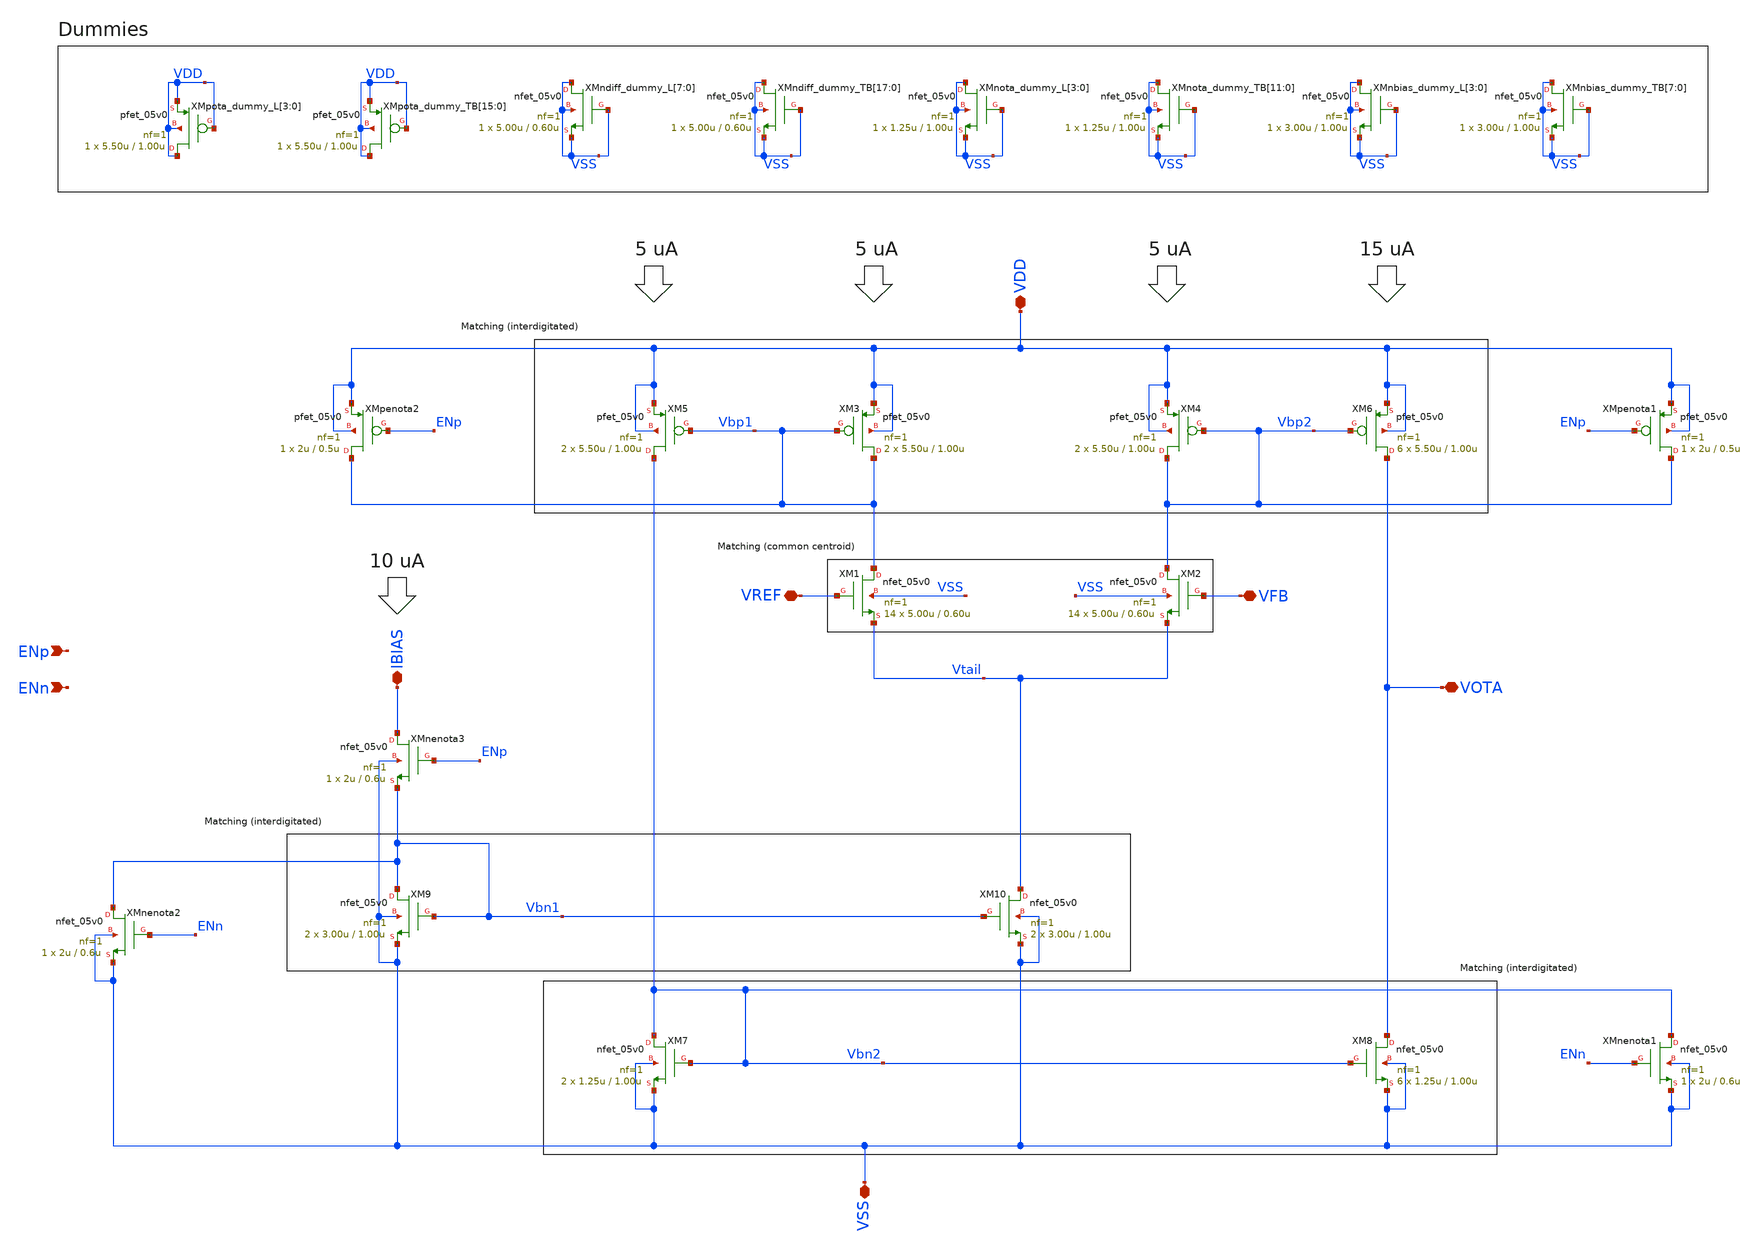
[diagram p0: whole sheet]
** sch_path: designs/libs/core_ldo/ldo_OTA/ldo_OTA.sch
**.subckt ldo_OTA VDD VSS VOTA VREF IBIAS VFB ENp ENn
*.iopin VDD
*.iopin VSS
*.iopin VOTA
*.iopin VREF
*.iopin IBIAS
*.iopin VFB
*.ipin ENp
*.ipin ENn
XM3 Vbp1 Vbp1 VDD VDD pfet_05v0 L=1.00u W=5.50u nf=1 ad='int((nf+1)/2) * W/nf * 0.18u' as='int((nf+2)/2) * W/nf * 0.18u'
+ pd='2*int((nf+1)/2) * (W/nf + 0.18u)' ps='2*int((nf+2)/2) * (W/nf + 0.18u)' nrd='0.18u / W' nrs='0.18u / W'
+ sa=0 sb=0 sd=0 m=2
XM4 Vbp2 Vbp2 VDD VDD pfet_05v0 L=1.00u W=5.50u nf=1 ad='int((nf+1)/2) * W/nf * 0.18u' as='int((nf+2)/2) * W/nf * 0.18u'
+ pd='2*int((nf+1)/2) * (W/nf + 0.18u)' ps='2*int((nf+2)/2) * (W/nf + 0.18u)' nrd='0.18u / W' nrs='0.18u / W'
+ sa=0 sb=0 sd=0 m=2
XM5 Vbn2 Vbp1 VDD VDD pfet_05v0 L=1.00u W=5.50u nf=1 ad='int((nf+1)/2) * W/nf * 0.18u' as='int((nf+2)/2) * W/nf * 0.18u'
+ pd='2*int((nf+1)/2) * (W/nf + 0.18u)' ps='2*int((nf+2)/2) * (W/nf + 0.18u)' nrd='0.18u / W' nrs='0.18u / W'
+ sa=0 sb=0 sd=0 m=2
XM6 VOTA Vbp2 VDD VDD pfet_05v0 L=1.00u W=5.50u nf=1 ad='int((nf+1)/2) * W/nf * 0.18u' as='int((nf+2)/2) * W/nf * 0.18u'
+ pd='2*int((nf+1)/2) * (W/nf + 0.18u)' ps='2*int((nf+2)/2) * (W/nf + 0.18u)' nrd='0.18u / W' nrs='0.18u / W'
+ sa=0 sb=0 sd=0 m=6
XM9 Vbn1 Vbn1 VSS VSS nfet_05v0 L=1.00u W=3.00u nf=1 ad='int((nf+1)/2) * W/nf * 0.18u' as='int((nf+2)/2) * W/nf * 0.18u'
+ pd='2*int((nf+1)/2) * (W/nf + 0.18u)' ps='2*int((nf+2)/2) * (W/nf + 0.18u)' nrd='0.18u / W' nrs='0.18u / W'
+ sa=0 sb=0 sd=0 m=2
XM10 Vtail Vbn1 VSS VSS nfet_05v0 L=1.00u W=3.00u nf=1 ad='int((nf+1)/2) * W/nf * 0.18u' as='int((nf+2)/2) * W/nf * 0.18u'
+ pd='2*int((nf+1)/2) * (W/nf + 0.18u)' ps='2*int((nf+2)/2) * (W/nf + 0.18u)' nrd='0.18u / W' nrs='0.18u / W'
+ sa=0 sb=0 sd=0 m=2
XM7 Vbn2 Vbn2 VSS VSS nfet_05v0 L=1.00u W=1.25u nf=1 ad='int((nf+1)/2) * W/nf * 0.18u' as='int((nf+2)/2) * W/nf * 0.18u'
+ pd='2*int((nf+1)/2) * (W/nf + 0.18u)' ps='2*int((nf+2)/2) * (W/nf + 0.18u)' nrd='0.18u / W' nrs='0.18u / W'
+ sa=0 sb=0 sd=0 m=2
XM8 VOTA Vbn2 VSS VSS nfet_05v0 L=1.00u W=1.25u nf=1 ad='int((nf+1)/2) * W/nf * 0.18u' as='int((nf+2)/2) * W/nf * 0.18u'
+ pd='2*int((nf+1)/2) * (W/nf + 0.18u)' ps='2*int((nf+2)/2) * (W/nf + 0.18u)' nrd='0.18u / W' nrs='0.18u / W'
+ sa=0 sb=0 sd=0 m=6
XM1 Vbp1 VREF Vtail VSS nfet_05v0 L=0.60u W=5.00u nf=1 ad='int((nf+1)/2) * W/nf * 0.18u' as='int((nf+2)/2) * W/nf * 0.18u'
+ pd='2*int((nf+1)/2) * (W/nf + 0.18u)' ps='2*int((nf+2)/2) * (W/nf + 0.18u)' nrd='0.18u / W' nrs='0.18u / W'
+ sa=0 sb=0 sd=0 m=14
XM2 Vbp2 VFB Vtail VSS nfet_05v0 L=0.60u W=5.00u nf=1 ad='int((nf+1)/2) * W/nf * 0.18u' as='int((nf+2)/2) * W/nf * 0.18u'
+ pd='2*int((nf+1)/2) * (W/nf + 0.18u)' ps='2*int((nf+2)/2) * (W/nf + 0.18u)' nrd='0.18u / W' nrs='0.18u / W'
+ sa=0 sb=0 sd=0 m=14
XMpota_dummy_L[3] VDD VDD VDD VDD pfet_05v0 L=1.00u W=5.50u nf=1 ad='int((nf+1)/2) * W/nf * 0.18u' as='int((nf+2)/2) * W/nf * 0.18u'
+ pd='2*int((nf+1)/2) * (W/nf + 0.18u)' ps='2*int((nf+2)/2) * (W/nf + 0.18u)' nrd='0.18u / W' nrs='0.18u / W'
+ sa=0 sb=0 sd=0 m=1
XMpota_dummy_L[2] VDD VDD VDD VDD pfet_05v0 L=1.00u W=5.50u nf=1 ad='int((nf+1)/2) * W/nf * 0.18u' as='int((nf+2)/2) * W/nf * 0.18u'
+ pd='2*int((nf+1)/2) * (W/nf + 0.18u)' ps='2*int((nf+2)/2) * (W/nf + 0.18u)' nrd='0.18u / W' nrs='0.18u / W'
+ sa=0 sb=0 sd=0 m=1
XMpota_dummy_L[1] VDD VDD VDD VDD pfet_05v0 L=1.00u W=5.50u nf=1 ad='int((nf+1)/2) * W/nf * 0.18u' as='int((nf+2)/2) * W/nf * 0.18u'
+ pd='2*int((nf+1)/2) * (W/nf + 0.18u)' ps='2*int((nf+2)/2) * (W/nf + 0.18u)' nrd='0.18u / W' nrs='0.18u / W'
+ sa=0 sb=0 sd=0 m=1
XMpota_dummy_L[0] VDD VDD VDD VDD pfet_05v0 L=1.00u W=5.50u nf=1 ad='int((nf+1)/2) * W/nf * 0.18u' as='int((nf+2)/2) * W/nf * 0.18u'
+ pd='2*int((nf+1)/2) * (W/nf + 0.18u)' ps='2*int((nf+2)/2) * (W/nf + 0.18u)' nrd='0.18u / W' nrs='0.18u / W'
+ sa=0 sb=0 sd=0 m=1
XMpota_dummy_TB[15] VDD VDD VDD VDD pfet_05v0 L=1.00u W=5.50u nf=1 ad='int((nf+1)/2) * W/nf * 0.18u'
+ as='int((nf+2)/2) * W/nf * 0.18u' pd='2*int((nf+1)/2) * (W/nf + 0.18u)' ps='2*int((nf+2)/2) * (W/nf + 0.18u)'
+ nrd='0.18u / W' nrs='0.18u / W' sa=0 sb=0 sd=0 m=1
XMpota_dummy_TB[14] VDD VDD VDD VDD pfet_05v0 L=1.00u W=5.50u nf=1 ad='int((nf+1)/2) * W/nf * 0.18u'
+ as='int((nf+2)/2) * W/nf * 0.18u' pd='2*int((nf+1)/2) * (W/nf + 0.18u)' ps='2*int((nf+2)/2) * (W/nf + 0.18u)'
+ nrd='0.18u / W' nrs='0.18u / W' sa=0 sb=0 sd=0 m=1
XMpota_dummy_TB[13] VDD VDD VDD VDD pfet_05v0 L=1.00u W=5.50u nf=1 ad='int((nf+1)/2) * W/nf * 0.18u'
+ as='int((nf+2)/2) * W/nf * 0.18u' pd='2*int((nf+1)/2) * (W/nf + 0.18u)' ps='2*int((nf+2)/2) * (W/nf + 0.18u)'
+ nrd='0.18u / W' nrs='0.18u / W' sa=0 sb=0 sd=0 m=1
XMpota_dummy_TB[12] VDD VDD VDD VDD pfet_05v0 L=1.00u W=5.50u nf=1 ad='int((nf+1)/2) * W/nf * 0.18u'
+ as='int((nf+2)/2) * W/nf * 0.18u' pd='2*int((nf+1)/2) * (W/nf + 0.18u)' ps='2*int((nf+2)/2) * (W/nf + 0.18u)'
+ nrd='0.18u / W' nrs='0.18u / W' sa=0 sb=0 sd=0 m=1
XMpota_dummy_TB[11] VDD VDD VDD VDD pfet_05v0 L=1.00u W=5.50u nf=1 ad='int((nf+1)/2) * W/nf * 0.18u'
+ as='int((nf+2)/2) * W/nf * 0.18u' pd='2*int((nf+1)/2) * (W/nf + 0.18u)' ps='2*int((nf+2)/2) * (W/nf + 0.18u)'
+ nrd='0.18u / W' nrs='0.18u / W' sa=0 sb=0 sd=0 m=1
XMpota_dummy_TB[10] VDD VDD VDD VDD pfet_05v0 L=1.00u W=5.50u nf=1 ad='int((nf+1)/2) * W/nf * 0.18u'
+ as='int((nf+2)/2) * W/nf * 0.18u' pd='2*int((nf+1)/2) * (W/nf + 0.18u)' ps='2*int((nf+2)/2) * (W/nf + 0.18u)'
+ nrd='0.18u / W' nrs='0.18u / W' sa=0 sb=0 sd=0 m=1
XMpota_dummy_TB[9] VDD VDD VDD VDD pfet_05v0 L=1.00u W=5.50u nf=1 ad='int((nf+1)/2) * W/nf * 0.18u' as='int((nf+2)/2) * W/nf * 0.18u'
+ pd='2*int((nf+1)/2) * (W/nf + 0.18u)' ps='2*int((nf+2)/2) * (W/nf + 0.18u)' nrd='0.18u / W' nrs='0.18u / W'
+ sa=0 sb=0 sd=0 m=1
XMpota_dummy_TB[8] VDD VDD VDD VDD pfet_05v0 L=1.00u W=5.50u nf=1 ad='int((nf+1)/2) * W/nf * 0.18u' as='int((nf+2)/2) * W/nf * 0.18u'
+ pd='2*int((nf+1)/2) * (W/nf + 0.18u)' ps='2*int((nf+2)/2) * (W/nf + 0.18u)' nrd='0.18u / W' nrs='0.18u / W'
+ sa=0 sb=0 sd=0 m=1
XMpota_dummy_TB[7] VDD VDD VDD VDD pfet_05v0 L=1.00u W=5.50u nf=1 ad='int((nf+1)/2) * W/nf * 0.18u' as='int((nf+2)/2) * W/nf * 0.18u'
+ pd='2*int((nf+1)/2) * (W/nf + 0.18u)' ps='2*int((nf+2)/2) * (W/nf + 0.18u)' nrd='0.18u / W' nrs='0.18u / W'
+ sa=0 sb=0 sd=0 m=1
XMpota_dummy_TB[6] VDD VDD VDD VDD pfet_05v0 L=1.00u W=5.50u nf=1 ad='int((nf+1)/2) * W/nf * 0.18u' as='int((nf+2)/2) * W/nf * 0.18u'
+ pd='2*int((nf+1)/2) * (W/nf + 0.18u)' ps='2*int((nf+2)/2) * (W/nf + 0.18u)' nrd='0.18u / W' nrs='0.18u / W'
+ sa=0 sb=0 sd=0 m=1
XMpota_dummy_TB[5] VDD VDD VDD VDD pfet_05v0 L=1.00u W=5.50u nf=1 ad='int((nf+1)/2) * W/nf * 0.18u' as='int((nf+2)/2) * W/nf * 0.18u'
+ pd='2*int((nf+1)/2) * (W/nf + 0.18u)' ps='2*int((nf+2)/2) * (W/nf + 0.18u)' nrd='0.18u / W' nrs='0.18u / W'
+ sa=0 sb=0 sd=0 m=1
XMpota_dummy_TB[4] VDD VDD VDD VDD pfet_05v0 L=1.00u W=5.50u nf=1 ad='int((nf+1)/2) * W/nf * 0.18u' as='int((nf+2)/2) * W/nf * 0.18u'
+ pd='2*int((nf+1)/2) * (W/nf + 0.18u)' ps='2*int((nf+2)/2) * (W/nf + 0.18u)' nrd='0.18u / W' nrs='0.18u / W'
+ sa=0 sb=0 sd=0 m=1
XMpota_dummy_TB[3] VDD VDD VDD VDD pfet_05v0 L=1.00u W=5.50u nf=1 ad='int((nf+1)/2) * W/nf * 0.18u' as='int((nf+2)/2) * W/nf * 0.18u'
+ pd='2*int((nf+1)/2) * (W/nf + 0.18u)' ps='2*int((nf+2)/2) * (W/nf + 0.18u)' nrd='0.18u / W' nrs='0.18u / W'
+ sa=0 sb=0 sd=0 m=1
XMpota_dummy_TB[2] VDD VDD VDD VDD pfet_05v0 L=1.00u W=5.50u nf=1 ad='int((nf+1)/2) * W/nf * 0.18u' as='int((nf+2)/2) * W/nf * 0.18u'
+ pd='2*int((nf+1)/2) * (W/nf + 0.18u)' ps='2*int((nf+2)/2) * (W/nf + 0.18u)' nrd='0.18u / W' nrs='0.18u / W'
+ sa=0 sb=0 sd=0 m=1
XMpota_dummy_TB[1] VDD VDD VDD VDD pfet_05v0 L=1.00u W=5.50u nf=1 ad='int((nf+1)/2) * W/nf * 0.18u' as='int((nf+2)/2) * W/nf * 0.18u'
+ pd='2*int((nf+1)/2) * (W/nf + 0.18u)' ps='2*int((nf+2)/2) * (W/nf + 0.18u)' nrd='0.18u / W' nrs='0.18u / W'
+ sa=0 sb=0 sd=0 m=1
XMpota_dummy_TB[0] VDD VDD VDD VDD pfet_05v0 L=1.00u W=5.50u nf=1 ad='int((nf+1)/2) * W/nf * 0.18u' as='int((nf+2)/2) * W/nf * 0.18u'
+ pd='2*int((nf+1)/2) * (W/nf + 0.18u)' ps='2*int((nf+2)/2) * (W/nf + 0.18u)' nrd='0.18u / W' nrs='0.18u / W'
+ sa=0 sb=0 sd=0 m=1
XMndiff_dummy_L[7] VSS VSS VSS VSS nfet_05v0 L=0.60u W=5.00u nf=1 ad='int((nf+1)/2) * W/nf * 0.18u' as='int((nf+2)/2) * W/nf * 0.18u'
+ pd='2*int((nf+1)/2) * (W/nf + 0.18u)' ps='2*int((nf+2)/2) * (W/nf + 0.18u)' nrd='0.18u / W' nrs='0.18u / W'
+ sa=0 sb=0 sd=0 m=1
XMndiff_dummy_L[6] VSS VSS VSS VSS nfet_05v0 L=0.60u W=5.00u nf=1 ad='int((nf+1)/2) * W/nf * 0.18u' as='int((nf+2)/2) * W/nf * 0.18u'
+ pd='2*int((nf+1)/2) * (W/nf + 0.18u)' ps='2*int((nf+2)/2) * (W/nf + 0.18u)' nrd='0.18u / W' nrs='0.18u / W'
+ sa=0 sb=0 sd=0 m=1
XMndiff_dummy_L[5] VSS VSS VSS VSS nfet_05v0 L=0.60u W=5.00u nf=1 ad='int((nf+1)/2) * W/nf * 0.18u' as='int((nf+2)/2) * W/nf * 0.18u'
+ pd='2*int((nf+1)/2) * (W/nf + 0.18u)' ps='2*int((nf+2)/2) * (W/nf + 0.18u)' nrd='0.18u / W' nrs='0.18u / W'
+ sa=0 sb=0 sd=0 m=1
XMndiff_dummy_L[4] VSS VSS VSS VSS nfet_05v0 L=0.60u W=5.00u nf=1 ad='int((nf+1)/2) * W/nf * 0.18u' as='int((nf+2)/2) * W/nf * 0.18u'
+ pd='2*int((nf+1)/2) * (W/nf + 0.18u)' ps='2*int((nf+2)/2) * (W/nf + 0.18u)' nrd='0.18u / W' nrs='0.18u / W'
+ sa=0 sb=0 sd=0 m=1
XMndiff_dummy_L[3] VSS VSS VSS VSS nfet_05v0 L=0.60u W=5.00u nf=1 ad='int((nf+1)/2) * W/nf * 0.18u' as='int((nf+2)/2) * W/nf * 0.18u'
+ pd='2*int((nf+1)/2) * (W/nf + 0.18u)' ps='2*int((nf+2)/2) * (W/nf + 0.18u)' nrd='0.18u / W' nrs='0.18u / W'
+ sa=0 sb=0 sd=0 m=1
XMndiff_dummy_L[2] VSS VSS VSS VSS nfet_05v0 L=0.60u W=5.00u nf=1 ad='int((nf+1)/2) * W/nf * 0.18u' as='int((nf+2)/2) * W/nf * 0.18u'
+ pd='2*int((nf+1)/2) * (W/nf + 0.18u)' ps='2*int((nf+2)/2) * (W/nf + 0.18u)' nrd='0.18u / W' nrs='0.18u / W'
+ sa=0 sb=0 sd=0 m=1
XMndiff_dummy_L[1] VSS VSS VSS VSS nfet_05v0 L=0.60u W=5.00u nf=1 ad='int((nf+1)/2) * W/nf * 0.18u' as='int((nf+2)/2) * W/nf * 0.18u'
+ pd='2*int((nf+1)/2) * (W/nf + 0.18u)' ps='2*int((nf+2)/2) * (W/nf + 0.18u)' nrd='0.18u / W' nrs='0.18u / W'
+ sa=0 sb=0 sd=0 m=1
XMndiff_dummy_L[0] VSS VSS VSS VSS nfet_05v0 L=0.60u W=5.00u nf=1 ad='int((nf+1)/2) * W/nf * 0.18u' as='int((nf+2)/2) * W/nf * 0.18u'
+ pd='2*int((nf+1)/2) * (W/nf + 0.18u)' ps='2*int((nf+2)/2) * (W/nf + 0.18u)' nrd='0.18u / W' nrs='0.18u / W'
+ sa=0 sb=0 sd=0 m=1
XMndiff_dummy_TB[17] VSS VSS VSS VSS nfet_05v0 L=0.60u W=5.00u nf=1 ad='int((nf+1)/2) * W/nf * 0.18u'
+ as='int((nf+2)/2) * W/nf * 0.18u' pd='2*int((nf+1)/2) * (W/nf + 0.18u)' ps='2*int((nf+2)/2) * (W/nf + 0.18u)'
+ nrd='0.18u / W' nrs='0.18u / W' sa=0 sb=0 sd=0 m=1
XMndiff_dummy_TB[16] VSS VSS VSS VSS nfet_05v0 L=0.60u W=5.00u nf=1 ad='int((nf+1)/2) * W/nf * 0.18u'
+ as='int((nf+2)/2) * W/nf * 0.18u' pd='2*int((nf+1)/2) * (W/nf + 0.18u)' ps='2*int((nf+2)/2) * (W/nf + 0.18u)'
+ nrd='0.18u / W' nrs='0.18u / W' sa=0 sb=0 sd=0 m=1
XMndiff_dummy_TB[15] VSS VSS VSS VSS nfet_05v0 L=0.60u W=5.00u nf=1 ad='int((nf+1)/2) * W/nf * 0.18u'
+ as='int((nf+2)/2) * W/nf * 0.18u' pd='2*int((nf+1)/2) * (W/nf + 0.18u)' ps='2*int((nf+2)/2) * (W/nf + 0.18u)'
+ nrd='0.18u / W' nrs='0.18u / W' sa=0 sb=0 sd=0 m=1
XMndiff_dummy_TB[14] VSS VSS VSS VSS nfet_05v0 L=0.60u W=5.00u nf=1 ad='int((nf+1)/2) * W/nf * 0.18u'
+ as='int((nf+2)/2) * W/nf * 0.18u' pd='2*int((nf+1)/2) * (W/nf + 0.18u)' ps='2*int((nf+2)/2) * (W/nf + 0.18u)'
+ nrd='0.18u / W' nrs='0.18u / W' sa=0 sb=0 sd=0 m=1
XMndiff_dummy_TB[13] VSS VSS VSS VSS nfet_05v0 L=0.60u W=5.00u nf=1 ad='int((nf+1)/2) * W/nf * 0.18u'
+ as='int((nf+2)/2) * W/nf * 0.18u' pd='2*int((nf+1)/2) * (W/nf + 0.18u)' ps='2*int((nf+2)/2) * (W/nf + 0.18u)'
+ nrd='0.18u / W' nrs='0.18u / W' sa=0 sb=0 sd=0 m=1
XMndiff_dummy_TB[12] VSS VSS VSS VSS nfet_05v0 L=0.60u W=5.00u nf=1 ad='int((nf+1)/2) * W/nf * 0.18u'
+ as='int((nf+2)/2) * W/nf * 0.18u' pd='2*int((nf+1)/2) * (W/nf + 0.18u)' ps='2*int((nf+2)/2) * (W/nf + 0.18u)'
+ nrd='0.18u / W' nrs='0.18u / W' sa=0 sb=0 sd=0 m=1
XMndiff_dummy_TB[11] VSS VSS VSS VSS nfet_05v0 L=0.60u W=5.00u nf=1 ad='int((nf+1)/2) * W/nf * 0.18u'
+ as='int((nf+2)/2) * W/nf * 0.18u' pd='2*int((nf+1)/2) * (W/nf + 0.18u)' ps='2*int((nf+2)/2) * (W/nf + 0.18u)'
+ nrd='0.18u / W' nrs='0.18u / W' sa=0 sb=0 sd=0 m=1
XMndiff_dummy_TB[10] VSS VSS VSS VSS nfet_05v0 L=0.60u W=5.00u nf=1 ad='int((nf+1)/2) * W/nf * 0.18u'
+ as='int((nf+2)/2) * W/nf * 0.18u' pd='2*int((nf+1)/2) * (W/nf + 0.18u)' ps='2*int((nf+2)/2) * (W/nf + 0.18u)'
+ nrd='0.18u / W' nrs='0.18u / W' sa=0 sb=0 sd=0 m=1
XMndiff_dummy_TB[9] VSS VSS VSS VSS nfet_05v0 L=0.60u W=5.00u nf=1 ad='int((nf+1)/2) * W/nf * 0.18u'
+ as='int((nf+2)/2) * W/nf * 0.18u' pd='2*int((nf+1)/2) * (W/nf + 0.18u)' ps='2*int((nf+2)/2) * (W/nf + 0.18u)'
+ nrd='0.18u / W' nrs='0.18u / W' sa=0 sb=0 sd=0 m=1
XMndiff_dummy_TB[8] VSS VSS VSS VSS nfet_05v0 L=0.60u W=5.00u nf=1 ad='int((nf+1)/2) * W/nf * 0.18u'
+ as='int((nf+2)/2) * W/nf * 0.18u' pd='2*int((nf+1)/2) * (W/nf + 0.18u)' ps='2*int((nf+2)/2) * (W/nf + 0.18u)'
+ nrd='0.18u / W' nrs='0.18u / W' sa=0 sb=0 sd=0 m=1
XMndiff_dummy_TB[7] VSS VSS VSS VSS nfet_05v0 L=0.60u W=5.00u nf=1 ad='int((nf+1)/2) * W/nf * 0.18u'
+ as='int((nf+2)/2) * W/nf * 0.18u' pd='2*int((nf+1)/2) * (W/nf + 0.18u)' ps='2*int((nf+2)/2) * (W/nf + 0.18u)'
+ nrd='0.18u / W' nrs='0.18u / W' sa=0 sb=0 sd=0 m=1
XMndiff_dummy_TB[6] VSS VSS VSS VSS nfet_05v0 L=0.60u W=5.00u nf=1 ad='int((nf+1)/2) * W/nf * 0.18u'
+ as='int((nf+2)/2) * W/nf * 0.18u' pd='2*int((nf+1)/2) * (W/nf + 0.18u)' ps='2*int((nf+2)/2) * (W/nf + 0.18u)'
+ nrd='0.18u / W' nrs='0.18u / W' sa=0 sb=0 sd=0 m=1
XMndiff_dummy_TB[5] VSS VSS VSS VSS nfet_05v0 L=0.60u W=5.00u nf=1 ad='int((nf+1)/2) * W/nf * 0.18u'
+ as='int((nf+2)/2) * W/nf * 0.18u' pd='2*int((nf+1)/2) * (W/nf + 0.18u)' ps='2*int((nf+2)/2) * (W/nf + 0.18u)'
+ nrd='0.18u / W' nrs='0.18u / W' sa=0 sb=0 sd=0 m=1
XMndiff_dummy_TB[4] VSS VSS VSS VSS nfet_05v0 L=0.60u W=5.00u nf=1 ad='int((nf+1)/2) * W/nf * 0.18u'
+ as='int((nf+2)/2) * W/nf * 0.18u' pd='2*int((nf+1)/2) * (W/nf + 0.18u)' ps='2*int((nf+2)/2) * (W/nf + 0.18u)'
+ nrd='0.18u / W' nrs='0.18u / W' sa=0 sb=0 sd=0 m=1
XMndiff_dummy_TB[3] VSS VSS VSS VSS nfet_05v0 L=0.60u W=5.00u nf=1 ad='int((nf+1)/2) * W/nf * 0.18u'
+ as='int((nf+2)/2) * W/nf * 0.18u' pd='2*int((nf+1)/2) * (W/nf + 0.18u)' ps='2*int((nf+2)/2) * (W/nf + 0.18u)'
+ nrd='0.18u / W' nrs='0.18u / W' sa=0 sb=0 sd=0 m=1
XMndiff_dummy_TB[2] VSS VSS VSS VSS nfet_05v0 L=0.60u W=5.00u nf=1 ad='int((nf+1)/2) * W/nf * 0.18u'
+ as='int((nf+2)/2) * W/nf * 0.18u' pd='2*int((nf+1)/2) * (W/nf + 0.18u)' ps='2*int((nf+2)/2) * (W/nf + 0.18u)'
+ nrd='0.18u / W' nrs='0.18u / W' sa=0 sb=0 sd=0 m=1
XMndiff_dummy_TB[1] VSS VSS VSS VSS nfet_05v0 L=0.60u W=5.00u nf=1 ad='int((nf+1)/2) * W/nf * 0.18u'
+ as='int((nf+2)/2) * W/nf * 0.18u' pd='2*int((nf+1)/2) * (W/nf + 0.18u)' ps='2*int((nf+2)/2) * (W/nf + 0.18u)'
+ nrd='0.18u / W' nrs='0.18u / W' sa=0 sb=0 sd=0 m=1
XMndiff_dummy_TB[0] VSS VSS VSS VSS nfet_05v0 L=0.60u W=5.00u nf=1 ad='int((nf+1)/2) * W/nf * 0.18u'
+ as='int((nf+2)/2) * W/nf * 0.18u' pd='2*int((nf+1)/2) * (W/nf + 0.18u)' ps='2*int((nf+2)/2) * (W/nf + 0.18u)'
+ nrd='0.18u / W' nrs='0.18u / W' sa=0 sb=0 sd=0 m=1
XMnota_dummy_L[3] VSS VSS VSS VSS nfet_05v0 L=1.00u W=1.25u nf=1 ad='int((nf+1)/2) * W/nf * 0.18u' as='int((nf+2)/2) * W/nf * 0.18u'
+ pd='2*int((nf+1)/2) * (W/nf + 0.18u)' ps='2*int((nf+2)/2) * (W/nf + 0.18u)' nrd='0.18u / W' nrs='0.18u / W'
+ sa=0 sb=0 sd=0 m=1
XMnota_dummy_L[2] VSS VSS VSS VSS nfet_05v0 L=1.00u W=1.25u nf=1 ad='int((nf+1)/2) * W/nf * 0.18u' as='int((nf+2)/2) * W/nf * 0.18u'
+ pd='2*int((nf+1)/2) * (W/nf + 0.18u)' ps='2*int((nf+2)/2) * (W/nf + 0.18u)' nrd='0.18u / W' nrs='0.18u / W'
+ sa=0 sb=0 sd=0 m=1
XMnota_dummy_L[1] VSS VSS VSS VSS nfet_05v0 L=1.00u W=1.25u nf=1 ad='int((nf+1)/2) * W/nf * 0.18u' as='int((nf+2)/2) * W/nf * 0.18u'
+ pd='2*int((nf+1)/2) * (W/nf + 0.18u)' ps='2*int((nf+2)/2) * (W/nf + 0.18u)' nrd='0.18u / W' nrs='0.18u / W'
+ sa=0 sb=0 sd=0 m=1
XMnota_dummy_L[0] VSS VSS VSS VSS nfet_05v0 L=1.00u W=1.25u nf=1 ad='int((nf+1)/2) * W/nf * 0.18u' as='int((nf+2)/2) * W/nf * 0.18u'
+ pd='2*int((nf+1)/2) * (W/nf + 0.18u)' ps='2*int((nf+2)/2) * (W/nf + 0.18u)' nrd='0.18u / W' nrs='0.18u / W'
+ sa=0 sb=0 sd=0 m=1
XMnota_dummy_TB[11] VSS VSS VSS VSS nfet_05v0 L=1.00u W=1.25u nf=1 ad='int((nf+1)/2) * W/nf * 0.18u'
+ as='int((nf+2)/2) * W/nf * 0.18u' pd='2*int((nf+1)/2) * (W/nf + 0.18u)' ps='2*int((nf+2)/2) * (W/nf + 0.18u)'
+ nrd='0.18u / W' nrs='0.18u / W' sa=0 sb=0 sd=0 m=1
XMnota_dummy_TB[10] VSS VSS VSS VSS nfet_05v0 L=1.00u W=1.25u nf=1 ad='int((nf+1)/2) * W/nf * 0.18u'
+ as='int((nf+2)/2) * W/nf * 0.18u' pd='2*int((nf+1)/2) * (W/nf + 0.18u)' ps='2*int((nf+2)/2) * (W/nf + 0.18u)'
+ nrd='0.18u / W' nrs='0.18u / W' sa=0 sb=0 sd=0 m=1
XMnota_dummy_TB[9] VSS VSS VSS VSS nfet_05v0 L=1.00u W=1.25u nf=1 ad='int((nf+1)/2) * W/nf * 0.18u' as='int((nf+2)/2) * W/nf * 0.18u'
+ pd='2*int((nf+1)/2) * (W/nf + 0.18u)' ps='2*int((nf+2)/2) * (W/nf + 0.18u)' nrd='0.18u / W' nrs='0.18u / W'
+ sa=0 sb=0 sd=0 m=1
XMnota_dummy_TB[8] VSS VSS VSS VSS nfet_05v0 L=1.00u W=1.25u nf=1 ad='int((nf+1)/2) * W/nf * 0.18u' as='int((nf+2)/2) * W/nf * 0.18u'
+ pd='2*int((nf+1)/2) * (W/nf + 0.18u)' ps='2*int((nf+2)/2) * (W/nf + 0.18u)' nrd='0.18u / W' nrs='0.18u / W'
+ sa=0 sb=0 sd=0 m=1
XMnota_dummy_TB[7] VSS VSS VSS VSS nfet_05v0 L=1.00u W=1.25u nf=1 ad='int((nf+1)/2) * W/nf * 0.18u' as='int((nf+2)/2) * W/nf * 0.18u'
+ pd='2*int((nf+1)/2) * (W/nf + 0.18u)' ps='2*int((nf+2)/2) * (W/nf + 0.18u)' nrd='0.18u / W' nrs='0.18u / W'
+ sa=0 sb=0 sd=0 m=1
XMnota_dummy_TB[6] VSS VSS VSS VSS nfet_05v0 L=1.00u W=1.25u nf=1 ad='int((nf+1)/2) * W/nf * 0.18u' as='int((nf+2)/2) * W/nf * 0.18u'
+ pd='2*int((nf+1)/2) * (W/nf + 0.18u)' ps='2*int((nf+2)/2) * (W/nf + 0.18u)' nrd='0.18u / W' nrs='0.18u / W'
+ sa=0 sb=0 sd=0 m=1
XMnota_dummy_TB[5] VSS VSS VSS VSS nfet_05v0 L=1.00u W=1.25u nf=1 ad='int((nf+1)/2) * W/nf * 0.18u' as='int((nf+2)/2) * W/nf * 0.18u'
+ pd='2*int((nf+1)/2) * (W/nf + 0.18u)' ps='2*int((nf+2)/2) * (W/nf + 0.18u)' nrd='0.18u / W' nrs='0.18u / W'
+ sa=0 sb=0 sd=0 m=1
XMnota_dummy_TB[4] VSS VSS VSS VSS nfet_05v0 L=1.00u W=1.25u nf=1 ad='int((nf+1)/2) * W/nf * 0.18u' as='int((nf+2)/2) * W/nf * 0.18u'
+ pd='2*int((nf+1)/2) * (W/nf + 0.18u)' ps='2*int((nf+2)/2) * (W/nf + 0.18u)' nrd='0.18u / W' nrs='0.18u / W'
+ sa=0 sb=0 sd=0 m=1
XMnota_dummy_TB[3] VSS VSS VSS VSS nfet_05v0 L=1.00u W=1.25u nf=1 ad='int((nf+1)/2) * W/nf * 0.18u' as='int((nf+2)/2) * W/nf * 0.18u'
+ pd='2*int((nf+1)/2) * (W/nf + 0.18u)' ps='2*int((nf+2)/2) * (W/nf + 0.18u)' nrd='0.18u / W' nrs='0.18u / W'
+ sa=0 sb=0 sd=0 m=1
XMnota_dummy_TB[2] VSS VSS VSS VSS nfet_05v0 L=1.00u W=1.25u nf=1 ad='int((nf+1)/2) * W/nf * 0.18u' as='int((nf+2)/2) * W/nf * 0.18u'
+ pd='2*int((nf+1)/2) * (W/nf + 0.18u)' ps='2*int((nf+2)/2) * (W/nf + 0.18u)' nrd='0.18u / W' nrs='0.18u / W'
+ sa=0 sb=0 sd=0 m=1
XMnota_dummy_TB[1] VSS VSS VSS VSS nfet_05v0 L=1.00u W=1.25u nf=1 ad='int((nf+1)/2) * W/nf * 0.18u' as='int((nf+2)/2) * W/nf * 0.18u'
+ pd='2*int((nf+1)/2) * (W/nf + 0.18u)' ps='2*int((nf+2)/2) * (W/nf + 0.18u)' nrd='0.18u / W' nrs='0.18u / W'
+ sa=0 sb=0 sd=0 m=1
XMnota_dummy_TB[0] VSS VSS VSS VSS nfet_05v0 L=1.00u W=1.25u nf=1 ad='int((nf+1)/2) * W/nf * 0.18u' as='int((nf+2)/2) * W/nf * 0.18u'
+ pd='2*int((nf+1)/2) * (W/nf + 0.18u)' ps='2*int((nf+2)/2) * (W/nf + 0.18u)' nrd='0.18u / W' nrs='0.18u / W'
+ sa=0 sb=0 sd=0 m=1
XMnbias_dummy_L[3] VSS VSS VSS VSS nfet_05v0 L=1.00u W=3.00u nf=1 ad='int((nf+1)/2) * W/nf * 0.18u' as='int((nf+2)/2) * W/nf * 0.18u'
+ pd='2*int((nf+1)/2) * (W/nf + 0.18u)' ps='2*int((nf+2)/2) * (W/nf + 0.18u)' nrd='0.18u / W' nrs='0.18u / W'
+ sa=0 sb=0 sd=0 m=1
XMnbias_dummy_L[2] VSS VSS VSS VSS nfet_05v0 L=1.00u W=3.00u nf=1 ad='int((nf+1)/2) * W/nf * 0.18u' as='int((nf+2)/2) * W/nf * 0.18u'
+ pd='2*int((nf+1)/2) * (W/nf + 0.18u)' ps='2*int((nf+2)/2) * (W/nf + 0.18u)' nrd='0.18u / W' nrs='0.18u / W'
+ sa=0 sb=0 sd=0 m=1
XMnbias_dummy_L[1] VSS VSS VSS VSS nfet_05v0 L=1.00u W=3.00u nf=1 ad='int((nf+1)/2) * W/nf * 0.18u' as='int((nf+2)/2) * W/nf * 0.18u'
+ pd='2*int((nf+1)/2) * (W/nf + 0.18u)' ps='2*int((nf+2)/2) * (W/nf + 0.18u)' nrd='0.18u / W' nrs='0.18u / W'
+ sa=0 sb=0 sd=0 m=1
XMnbias_dummy_L[0] VSS VSS VSS VSS nfet_05v0 L=1.00u W=3.00u nf=1 ad='int((nf+1)/2) * W/nf * 0.18u' as='int((nf+2)/2) * W/nf * 0.18u'
+ pd='2*int((nf+1)/2) * (W/nf + 0.18u)' ps='2*int((nf+2)/2) * (W/nf + 0.18u)' nrd='0.18u / W' nrs='0.18u / W'
+ sa=0 sb=0 sd=0 m=1
XMnbias_dummy_TB[7] VSS VSS VSS VSS nfet_05v0 L=1.00u W=3.00u nf=1 ad='int((nf+1)/2) * W/nf * 0.18u'
+ as='int((nf+2)/2) * W/nf * 0.18u' pd='2*int((nf+1)/2) * (W/nf + 0.18u)' ps='2*int((nf+2)/2) * (W/nf + 0.18u)'
+ nrd='0.18u / W' nrs='0.18u / W' sa=0 sb=0 sd=0 m=1
XMnbias_dummy_TB[6] VSS VSS VSS VSS nfet_05v0 L=1.00u W=3.00u nf=1 ad='int((nf+1)/2) * W/nf * 0.18u'
+ as='int((nf+2)/2) * W/nf * 0.18u' pd='2*int((nf+1)/2) * (W/nf + 0.18u)' ps='2*int((nf+2)/2) * (W/nf + 0.18u)'
+ nrd='0.18u / W' nrs='0.18u / W' sa=0 sb=0 sd=0 m=1
XMnbias_dummy_TB[5] VSS VSS VSS VSS nfet_05v0 L=1.00u W=3.00u nf=1 ad='int((nf+1)/2) * W/nf * 0.18u'
+ as='int((nf+2)/2) * W/nf * 0.18u' pd='2*int((nf+1)/2) * (W/nf + 0.18u)' ps='2*int((nf+2)/2) * (W/nf + 0.18u)'
+ nrd='0.18u / W' nrs='0.18u / W' sa=0 sb=0 sd=0 m=1
XMnbias_dummy_TB[4] VSS VSS VSS VSS nfet_05v0 L=1.00u W=3.00u nf=1 ad='int((nf+1)/2) * W/nf * 0.18u'
+ as='int((nf+2)/2) * W/nf * 0.18u' pd='2*int((nf+1)/2) * (W/nf + 0.18u)' ps='2*int((nf+2)/2) * (W/nf + 0.18u)'
+ nrd='0.18u / W' nrs='0.18u / W' sa=0 sb=0 sd=0 m=1
XMnbias_dummy_TB[3] VSS VSS VSS VSS nfet_05v0 L=1.00u W=3.00u nf=1 ad='int((nf+1)/2) * W/nf * 0.18u'
+ as='int((nf+2)/2) * W/nf * 0.18u' pd='2*int((nf+1)/2) * (W/nf + 0.18u)' ps='2*int((nf+2)/2) * (W/nf + 0.18u)'
+ nrd='0.18u / W' nrs='0.18u / W' sa=0 sb=0 sd=0 m=1
XMnbias_dummy_TB[2] VSS VSS VSS VSS nfet_05v0 L=1.00u W=3.00u nf=1 ad='int((nf+1)/2) * W/nf * 0.18u'
+ as='int((nf+2)/2) * W/nf * 0.18u' pd='2*int((nf+1)/2) * (W/nf + 0.18u)' ps='2*int((nf+2)/2) * (W/nf + 0.18u)'
+ nrd='0.18u / W' nrs='0.18u / W' sa=0 sb=0 sd=0 m=1
XMnbias_dummy_TB[1] VSS VSS VSS VSS nfet_05v0 L=1.00u W=3.00u nf=1 ad='int((nf+1)/2) * W/nf * 0.18u'
+ as='int((nf+2)/2) * W/nf * 0.18u' pd='2*int((nf+1)/2) * (W/nf + 0.18u)' ps='2*int((nf+2)/2) * (W/nf + 0.18u)'
+ nrd='0.18u / W' nrs='0.18u / W' sa=0 sb=0 sd=0 m=1
XMnbias_dummy_TB[0] VSS VSS VSS VSS nfet_05v0 L=1.00u W=3.00u nf=1 ad='int((nf+1)/2) * W/nf * 0.18u'
+ as='int((nf+2)/2) * W/nf * 0.18u' pd='2*int((nf+1)/2) * (W/nf + 0.18u)' ps='2*int((nf+2)/2) * (W/nf + 0.18u)'
+ nrd='0.18u / W' nrs='0.18u / W' sa=0 sb=0 sd=0 m=1
XMpenota1 Vbp2 ENp VDD VDD pfet_05v0 L=0.5u W=2u nf=1 ad='int((nf+1)/2) * W/nf * 0.18u' as='int((nf+2)/2) * W/nf * 0.18u'
+ pd='2*int((nf+1)/2) * (W/nf + 0.18u)' ps='2*int((nf+2)/2) * (W/nf + 0.18u)' nrd='0.18u / W' nrs='0.18u / W'
+ sa=0 sb=0 sd=0 m=1
XMpenota2 Vbp1 ENp VDD VDD pfet_05v0 L=0.5u W=2u nf=1 ad='int((nf+1)/2) * W/nf * 0.18u' as='int((nf+2)/2) * W/nf * 0.18u'
+ pd='2*int((nf+1)/2) * (W/nf + 0.18u)' ps='2*int((nf+2)/2) * (W/nf + 0.18u)' nrd='0.18u / W' nrs='0.18u / W'
+ sa=0 sb=0 sd=0 m=1
XMnenota1 Vbn2 ENn VSS VSS nfet_05v0 L=0.6u W=2u nf=1 ad='int((nf+1)/2) * W/nf * 0.18u' as='int((nf+2)/2) * W/nf * 0.18u'
+ pd='2*int((nf+1)/2) * (W/nf + 0.18u)' ps='2*int((nf+2)/2) * (W/nf + 0.18u)' nrd='0.18u / W' nrs='0.18u / W'
+ sa=0 sb=0 sd=0 m=1
XMnenota2 Vbn1 ENn VSS VSS nfet_05v0 L=0.6u W=2u nf=1 ad='int((nf+1)/2) * W/nf * 0.18u' as='int((nf+2)/2) * W/nf * 0.18u'
+ pd='2*int((nf+1)/2) * (W/nf + 0.18u)' ps='2*int((nf+2)/2) * (W/nf + 0.18u)' nrd='0.18u / W' nrs='0.18u / W'
+ sa=0 sb=0 sd=0 m=1
XMnenota3 IBIAS ENp Vbn1 VSS nfet_05v0 L=0.6u W=2u nf=1 ad='int((nf+1)/2) * W/nf * 0.18u' as='int((nf+2)/2) * W/nf * 0.18u'
+ pd='2*int((nf+1)/2) * (W/nf + 0.18u)' ps='2*int((nf+2)/2) * (W/nf + 0.18u)' nrd='0.18u / W' nrs='0.18u / W'
+ sa=0 sb=0 sd=0 m=1
**.ends
.end
